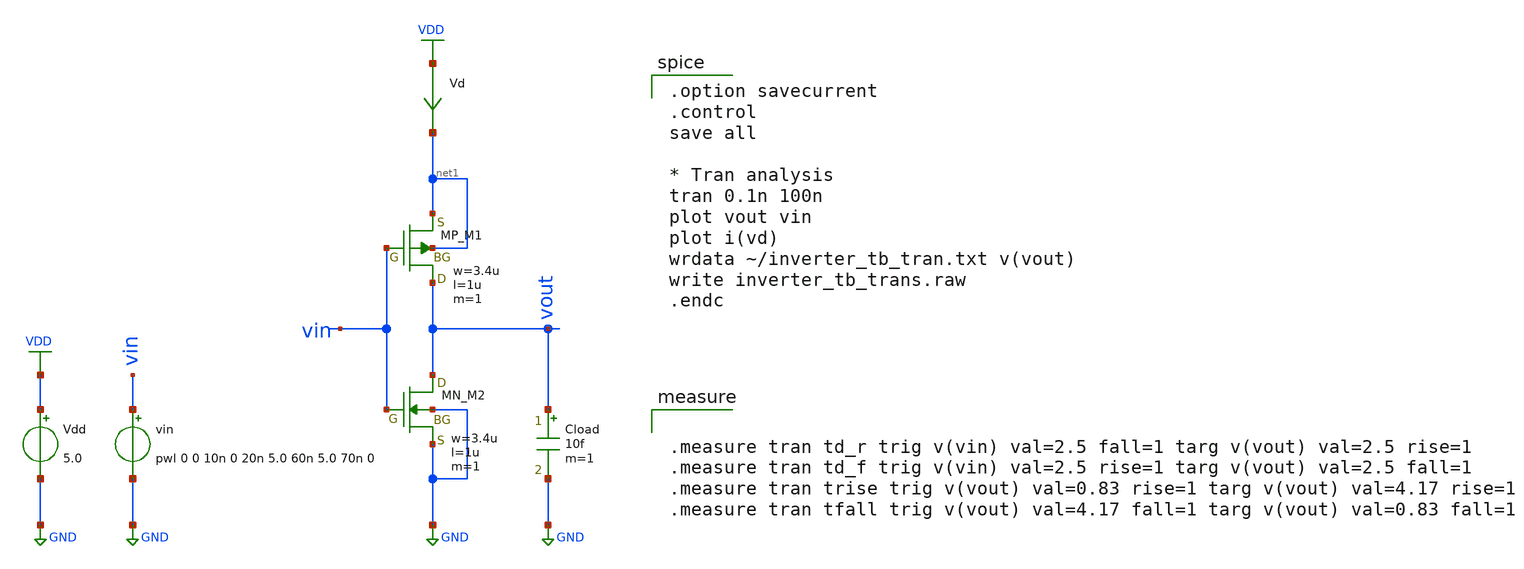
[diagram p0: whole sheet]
** sch_path: inverter/kato/inverter_kato1_tb_trans.sch
**.subckt inverter_kato1_tb_trans
XM1 vout vin net1 net1 PMOS w=3.4u l=1u nrd=0 nrs=0 m=1
XM2 vout vin GND GND NMOS w=3.4u l=1u nrd=0 nrs=0 m=1
Cload vout GND 10f m=1
Vdd VDD GND 5.0
Vd VDD net1 0
.save i(vd)
vin vin GND pwl 0 0 10n 0 20n 5.0 60n 5.0 70n 0
**** begin user architecture code
 .include $::LIB/ip62_models

.option savecurrent
.control
save all

* Tran analysis
tran 0.1n 100n
plot vout vin
plot i(vd)
wrdata ~/inverter_tb_tran.txt v(vout)
write inverter_tb_trans.raw
.endc



.measure tran td_r trig v(vin) val=2.5 fall=1 targ v(vout) val=2.5 rise=1
.measure tran td_f trig v(vin) val=2.5 rise=1 targ v(vout) val=2.5 fall=1
.measure tran trise trig v(vout) val=0.83 rise=1 targ v(vout) val=4.17 rise=1
.measure tran tfall trig v(vout) val=4.17 fall=1 targ v(vout) val=0.83 fall=1


**** end user architecture code
**.ends
.GLOBAL GND
.GLOBAL VDD
.end
